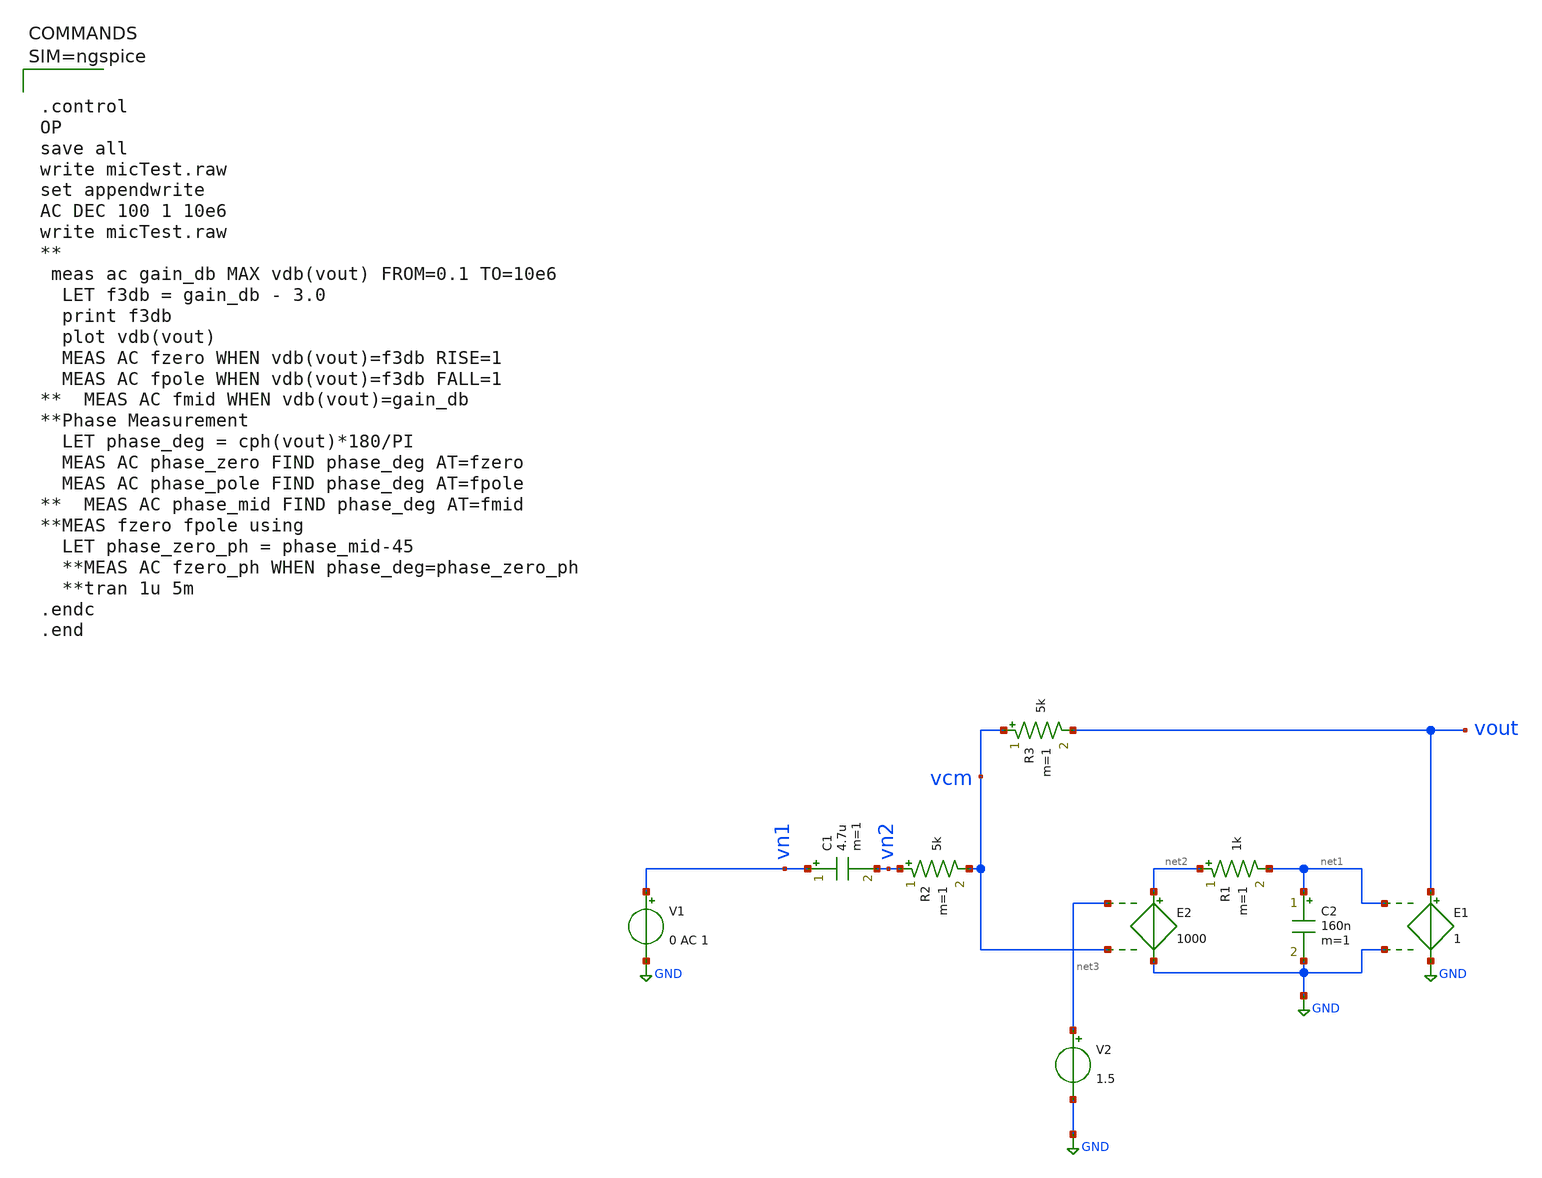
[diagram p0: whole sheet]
** sch_path: xschem/micNew.sch
**.subckt micNew
V1 vn1 GND 0 AC 1
C1 vn1 vn2 4.7u m=1
R2 vn2 vcm 5k m=1
R3 vcm vout 5k m=1
E1 vout GND net1 GND 1
E2 net2 GND net3 vcm 1000
R1 net2 net1 1k m=1
C2 net1 GND 160n m=1
V2 net3 GND 1.5
**** begin user architecture code



.control
OP
save all
write micTest.raw
set appendwrite
AC DEC 100 1 10e6
write micTest.raw
**
 meas ac gain_db MAX vdb(vout) FROM=0.1 TO=10e6
  LET f3db = gain_db - 3.0
  print f3db
  plot vdb(vout)
  MEAS AC fzero WHEN vdb(vout)=f3db RISE=1
  MEAS AC fpole WHEN vdb(vout)=f3db FALL=1
**  MEAS AC fmid WHEN vdb(vout)=gain_db
**Phase Measurement
  LET phase_deg = cph(vout)*180/PI
  MEAS AC phase_zero FIND phase_deg AT=fzero
  MEAS AC phase_pole FIND phase_deg AT=fpole
**  MEAS AC phase_mid FIND phase_deg AT=fmid
**MEAS fzero fpole using
  LET phase_zero_ph = phase_mid-45
  **MEAS AC fzero_ph WHEN phase_deg=phase_zero_ph
  **tran 1u 5m
.endc
.end



**** end user architecture code
**.ends
.GLOBAL GND
.end
